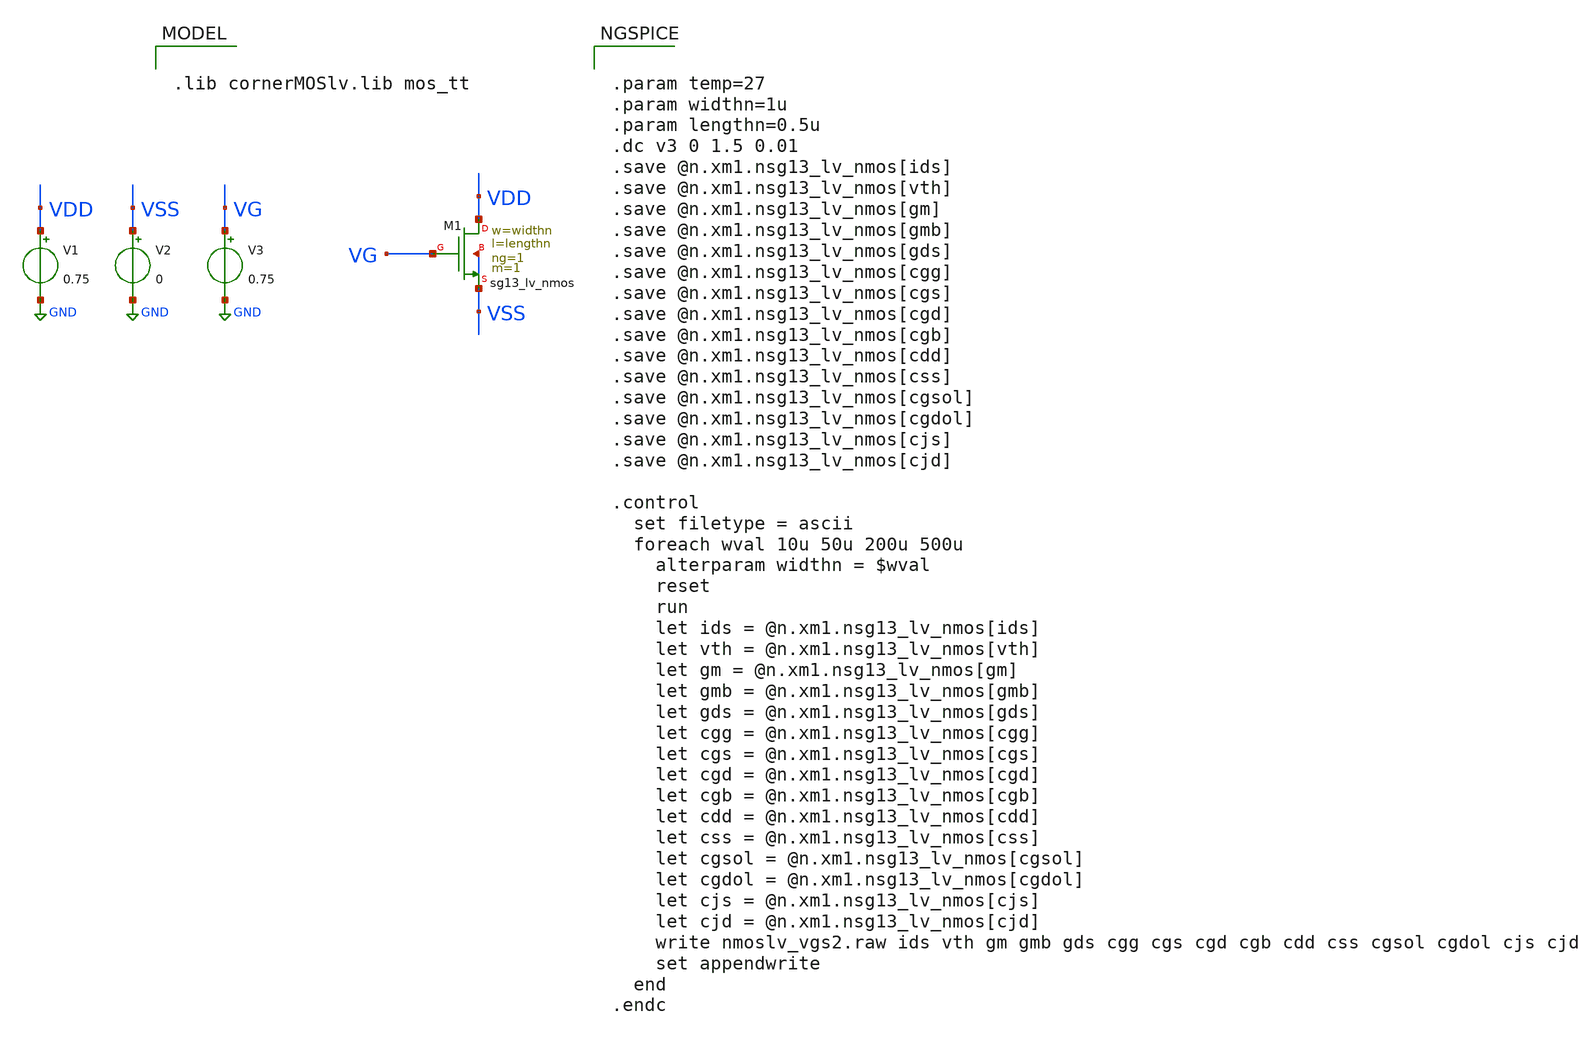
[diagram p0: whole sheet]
** sch_path: analog/tb/tb_nmos_lv_vgs.sch
**.subckt tb_nmos_lv_vgs
V1 VDD GND 0.75
V2 VSS GND 0
V3 VG GND 0.75
XM1 VDD VG VSS VSS sg13_lv_nmos w=widthn l=lengthn ng=1 m=1 mm_ok=1
**** begin user architecture code


.param temp=27
.param widthn=1u
.param lengthn=0.5u
.dc v3 0 1.5 0.01
.save @n.xm1.nsg13_lv_nmos[ids]
.save @n.xm1.nsg13_lv_nmos[vth]
.save @n.xm1.nsg13_lv_nmos[gm]
.save @n.xm1.nsg13_lv_nmos[gmb]
.save @n.xm1.nsg13_lv_nmos[gds]
.save @n.xm1.nsg13_lv_nmos[cgg]
.save @n.xm1.nsg13_lv_nmos[cgs]
.save @n.xm1.nsg13_lv_nmos[cgd]
.save @n.xm1.nsg13_lv_nmos[cgb]
.save @n.xm1.nsg13_lv_nmos[cdd]
.save @n.xm1.nsg13_lv_nmos[css]
.save @n.xm1.nsg13_lv_nmos[cgsol]
.save @n.xm1.nsg13_lv_nmos[cgdol]
.save @n.xm1.nsg13_lv_nmos[cjs]
.save @n.xm1.nsg13_lv_nmos[cjd]

.control
  set filetype = ascii
  foreach wval 10u 50u 200u 500u
    alterparam widthn = $wval
    reset
    run
    let ids = @n.xm1.nsg13_lv_nmos[ids]
    let vth = @n.xm1.nsg13_lv_nmos[vth]
    let gm = @n.xm1.nsg13_lv_nmos[gm]
    let gmb = @n.xm1.nsg13_lv_nmos[gmb]
    let gds = @n.xm1.nsg13_lv_nmos[gds]
    let cgg = @n.xm1.nsg13_lv_nmos[cgg]
    let cgs = @n.xm1.nsg13_lv_nmos[cgs]
    let cgd = @n.xm1.nsg13_lv_nmos[cgd]
    let cgb = @n.xm1.nsg13_lv_nmos[cgb]
    let cdd = @n.xm1.nsg13_lv_nmos[cdd]
    let css = @n.xm1.nsg13_lv_nmos[css]
    let cgsol = @n.xm1.nsg13_lv_nmos[cgsol]
    let cgdol = @n.xm1.nsg13_lv_nmos[cgdol]
    let cjs = @n.xm1.nsg13_lv_nmos[cjs]
    let cjd = @n.xm1.nsg13_lv_nmos[cjd]
    write nmoslv_vgs2.raw ids vth gm gmb gds cgg cgs cgd cgb cdd css cgsol cgdol cjs cjd
    set appendwrite
  end
.endc





.lib cornerMOSlv.lib mos_tt


**** end user architecture code
**.ends
.GLOBAL GND
.end
